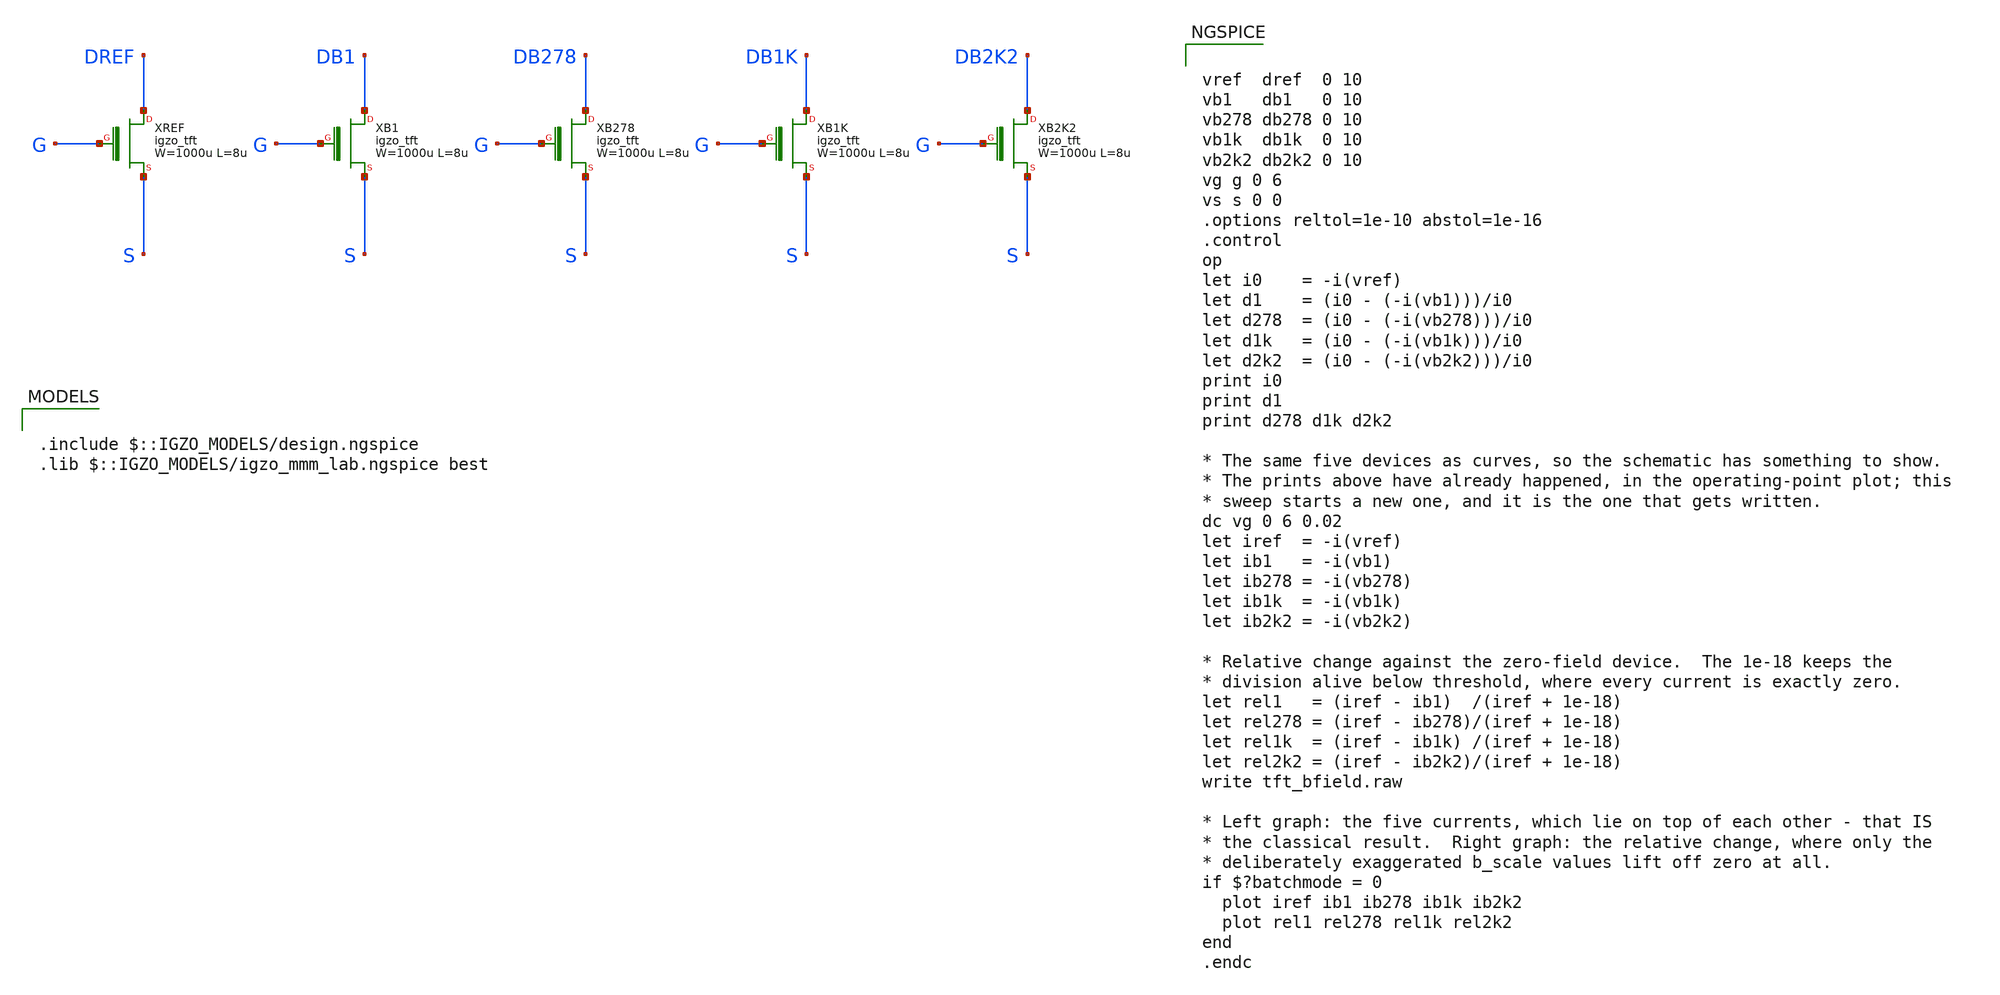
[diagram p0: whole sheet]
** sch_path: libs.tech/xschem/tests/tft_bfield.sch
**.subckt tft_bfield
XXREF DREF G S igzo_tft W=1000u L=8u ov=5u nf=1 m=1
XXB1 DB1 G S igzo_tft W=1000u L=8u ov=5u nf=1 m=1
XXB278 DB278 G S igzo_tft W=1000u L=8u ov=5u nf=1 m=1
XXB1K DB1K G S igzo_tft W=1000u L=8u ov=5u nf=1 m=1
XXB2K2 DB2K2 G S igzo_tft W=1000u L=8u ov=5u nf=1 m=1
**** begin user architecture code

.include $::IGZO_MODELS/design.ngspice
.lib $::IGZO_MODELS/igzo_mmm_lab.ngspice best



vref  dref  0 10
vb1   db1   0 10
vb278 db278 0 10
vb1k  db1k  0 10
vb2k2 db2k2 0 10
vg g 0 6
vs s 0 0
.options reltol=1e-10 abstol=1e-16
.control
op
let i0    = -i(vref)
let d1    = (i0 - (-i(vb1)))/i0
let d278  = (i0 - (-i(vb278)))/i0
let d1k   = (i0 - (-i(vb1k)))/i0
let d2k2  = (i0 - (-i(vb2k2)))/i0
print i0
print d1
print d278 d1k d2k2

* The same five devices as curves, so the schematic has something to show.
* The prints above have already happened, in the operating-point plot; this
* sweep starts a new one, and it is the one that gets written.
dc vg 0 6 0.02
let iref  = -i(vref)
let ib1   = -i(vb1)
let ib278 = -i(vb278)
let ib1k  = -i(vb1k)
let ib2k2 = -i(vb2k2)

* Relative change against the zero-field device.  The 1e-18 keeps the
* division alive below threshold, where every current is exactly zero.
let rel1   = (iref - ib1)  /(iref + 1e-18)
let rel278 = (iref - ib278)/(iref + 1e-18)
let rel1k  = (iref - ib1k) /(iref + 1e-18)
let rel2k2 = (iref - ib2k2)/(iref + 1e-18)
write tft_bfield.raw

* Left graph: the five currents, which lie on top of each other - that IS
* the classical result.  Right graph: the relative change, where only the
* deliberately exaggerated b_scale values lift off zero at all.
if $?batchmode = 0
  plot iref ib1 ib278 ib1k ib2k2
  plot rel1 rel278 rel1k rel2k2
end
.endc


**** end user architecture code
**.ends
.end
